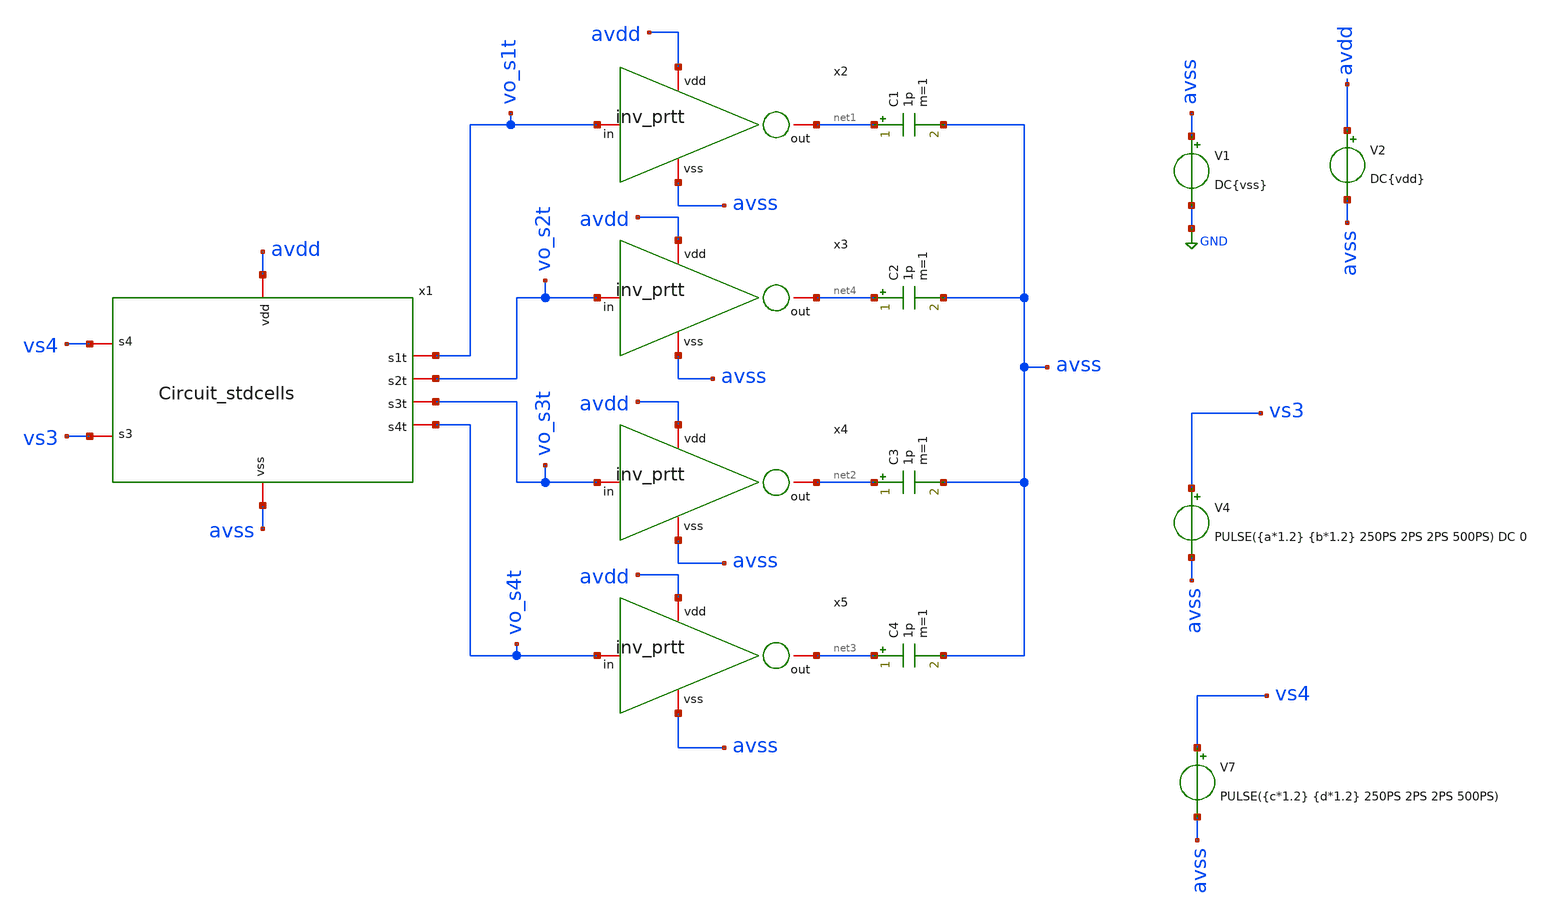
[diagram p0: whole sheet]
** sch_path: BinarytoThermo/tb_Circuit_stdcells_tran.sch
**.subckt tb_Circuit_stdcells_tran
C1 net1 avss 1p m=1
C2 net4 avss 1p m=1
C3 net2 avss 1p m=1
C4 net3 avss 1p m=1
V1 avss GND DC{vss}
V2 avdd avss DC{vdd}
V4 vs3 avss PULSE({a*1.2} {b*1.2} 250PS 2PS 2PS 500PS) DC 0
x1 vs4 vs3 vo_s1t vo_s2t vo_s3t avdd vo_s4t avss Circuit_stdcells
x2 avdd vo_s1t net1 avss inv_prtt
x3 avdd vo_s2t net4 avss inv_prtt
x4 avdd vo_s3t net2 avss inv_prtt
x5 avdd vo_s4t net3 avss inv_prtt
V7 vs4 avss PULSE({c*1.2} {d*1.2} 250PS 2PS 2PS 500PS)
**** begin user architecture code



* Circuit Parameters
.param vdd = 1.2
.param vss = 0.0
.param a=0
.param b=0
.param c=0
.param d=1
.param Tclk = 500P
.options TEMP = 65.0

* Include Models
.lib /foss/pdks/ihp-sg13g2/libs.tech/ngspice/models/cornerMOSlv.lib mos_tt
.lib /foss/pdks/ihp-sg13g2/libs.tech/ngspice/models/cornerMOShv.lib mos_tt
.lib /foss/pdks/ihp-sg13g2/libs.tech/ngspice/models/cornerHBT.lib hbt_typ
.lib /foss/pdks/ihp-sg13g2/libs.tech/ngspice/models/cornerRES.lib res_typ


* OP Parameters & Singals to save
.save all

*Simulations
.control
set output_path = tb_termopi_tran/
	* Desde (s3,s4)=00 a 01
	tran 0.2PS 750PS
	setplot tran1
	plot vs3 vs4 vo_s3t ylabel vout xlabel vin
	set filetype = ascii
	write {$output_path}tran00to01.raw V(vo_s3t) V(vs3) V(vs4)
	* Desde (s3,s4)=00 a 10
	alterparam d=0
	alterparam b=1
	reset
	tran 0.2PS 750PS
	setplot tran2
	plot vs3 vs4 vo_s2t vo_s3t ylabel vout xlabel vin
	set filetype = ascii
	write {$output_path}tran00to10.raw V(vo_s2t) V(vo_s3t) V(vs3) V(vs4)
	* Desde (s3,s4)=00 a 11
	alterparam d = 1
	reset
	tran 0.2PS 750PS
	setplot tran3
	plot vs3 vs4 vo_s1t vo_s2t vo_s3t ylabel vout xlabel vin
	set filetype = ascii
	write {$output_path}tran00to11.raw V(vo_s1t) V(vo_s2t) V(vo_s3t) V(vs3) V(vs4)
	* Desde (s3,s4)=01 a 10
	alterparam c=1
	alterparam d=0
	reset
	tran 0.2PS 750PS
	setplot tran4
	plot vs3 vs4 vo_s2t ylabel vout xlabel vin
	set filetype = ascii
	write {$output_path}tran01to10.raw V(vo_s2t) V(vs3) V(vs4)
	* Desde (s3,s4)=01 a 11
	alterparam a=0
	alterparam b=1
	alterparam d=1
	reset
	tran 0.2PS 750PS
	setplot tran5
	plot vs3 vs4 vo_s1t vo_s2t ylabel vout xlabel vin
	set filetype = ascii
	write {$output_path}tran01to11.raw V(vo_s1t) V(vo_s2t) V(vs3) V(vs4)
	* Desde (s3,s4)=10 a 11
	alterparam a=1
	alterparam c=0
	alterparam d=1
	reset
	tran 0.2PS 750PS
	setplot tran6
	plot vs3 vs4 vo_s1t ylabel vout xlabel vin ylimit 0 1.2
	set filetype = ascii
	write {$output_path}tran10to11.raw V(vo_s1t) V(vs3) V(vs4)
.endc
.end

**** end user architecture code
**.ends
.GLOBAL GND
.end
